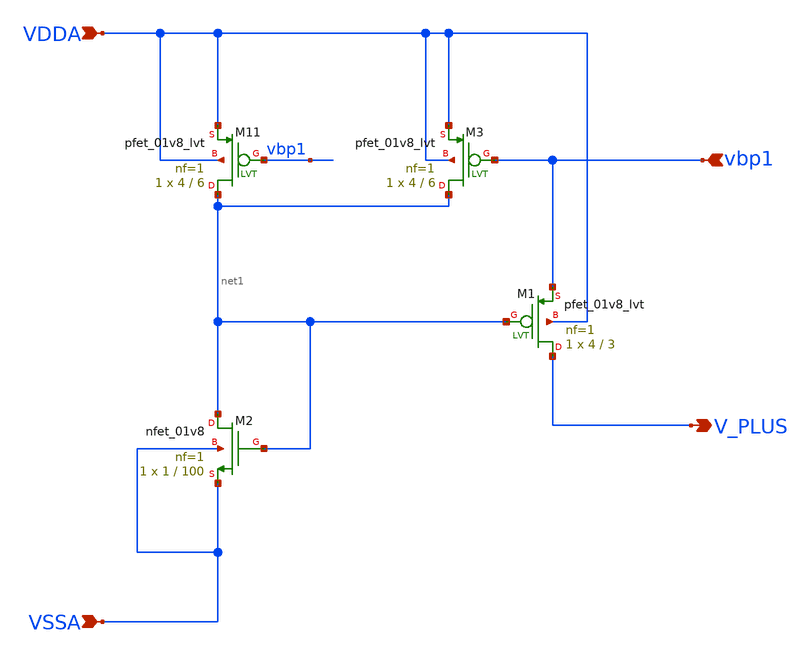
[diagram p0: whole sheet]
** sch_path: lef/bg2_startup.sch
**.subckt bg2_startup VDDA VSSA vbp1 V_PLUS
*.ipin VDDA
*.ipin VSSA
*.ipin vbp1
*.opin V_PLUS
XM1 V_PLUS net1 vbp1 VDDA sky130_fd_pr__pfet_01v8_lvt L=3 W=4 nf=1 ad='int((1 + 1)/2) * 4 / 1 * 0.29'
+ as='int((1 + 2)/2) * 4 / 1 * 0.29' pd='2*int((1 + 1)/2) * (4 / 1 + 0.29)' ps='2*int((1 + 2)/2) * (4 / 1 + 0.29)'
+ nrd='0.29 / 4 ' nrs='0.29 / 4 ' sa=0 sb=0 sd=0 mult=1 m=1
XM2 net1 net1 VSSA VSSA sky130_fd_pr__nfet_01v8 L=100 W=1 nf=1 ad='int((1 + 1)/2) * 1 / 1 * 0.29' as='int((1 + 2)/2) * 1 / 1 * 0.29'
+ pd='2*int((1 + 1)/2) * (1 / 1 + 0.29)' ps='2*int((1 + 2)/2) * (1 / 1 + 0.29)' nrd='0.29 / 1 ' nrs='0.29 / 1 '
+ sa=0 sb=0 sd=0 mult=1 m=1
XM11 net1 vbp1 VDDA VDDA sky130_fd_pr__pfet_01v8_lvt L=6 W=4 nf=1 ad='int((1 + 1)/2) * 4 / 1 * 0.29'
+ as='int((1 + 2)/2) * 4 / 1 * 0.29' pd='2*int((1 + 1)/2) * (4 / 1 + 0.29)' ps='2*int((1 + 2)/2) * (4 / 1 + 0.29)'
+ nrd='0.29 / 4 ' nrs='0.29 / 4 ' sa=0 sb=0 sd=0 mult=1 m=1
XM3 net1 vbp1 VDDA VDDA sky130_fd_pr__pfet_01v8_lvt L=6 W=4 nf=1 ad='int((1 + 1)/2) * 4 / 1 * 0.29' as='int((1 + 2)/2) * 4 / 1 * 0.29'
+ pd='2*int((1 + 1)/2) * (4 / 1 + 0.29)' ps='2*int((1 + 2)/2) * (4 / 1 + 0.29)' nrd='0.29 / 4 ' nrs='0.29 / 4 '
+ sa=0 sb=0 sd=0 mult=1 m=1
**.ends
.end
